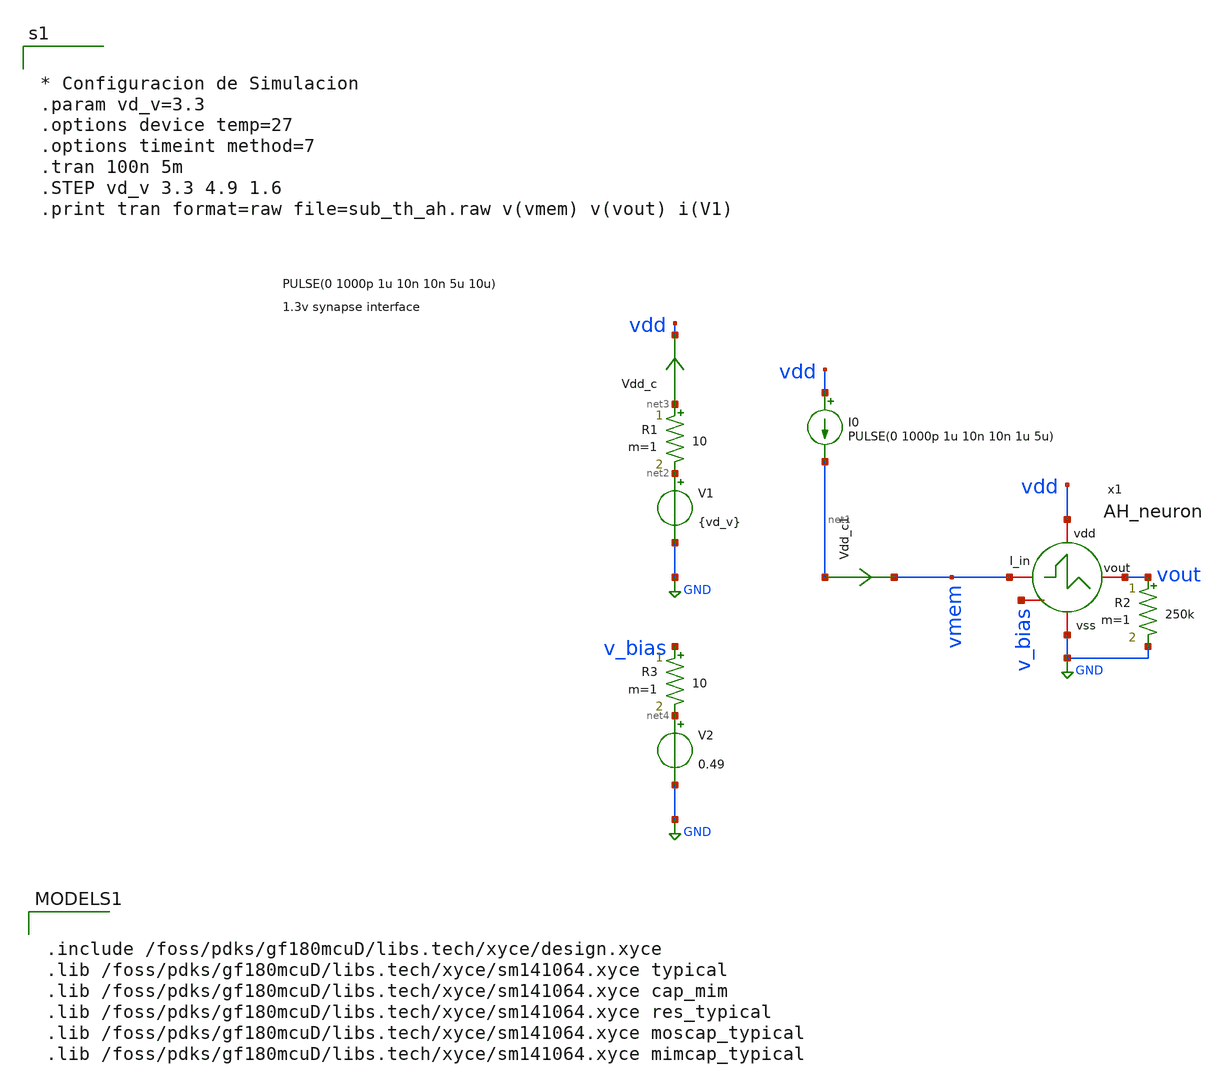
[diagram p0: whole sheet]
** sch_path: designs/libs/tb_core_analogs/tb_AH_neuron/AH_neuron.sch
**.subckt AH_neuron
V1 net2 GND {vd_v}
Vdd_c net3 vdd 0
.save i(vdd_c)
I0 vdd net1 PULSE(0 1000p 1u 10n 10n 1u 5u)
x1 vdd vmem vout GND v_bias AH_neuron
R1 net3 net2 10 m=1
R2 vout GND 250k m=1
Vdd_c1 net1 vmem 0
.save i(vdd_c1)
V2 net4 GND 0.49
R3 v_bias net4 10 m=1
**** begin user architecture code


* Configuracion de Simulacion
.param vd_v=3.3
.options device temp=27
.options timeint method=7
.tran 100n 5m
.STEP vd_v 3.3 4.9 1.6
.print tran format=raw file=sub_th_ah.raw v(vmem) v(vout) i(V1)



.include /foss/pdks/gf180mcuD/libs.tech/xyce/design.xyce
.lib /foss/pdks/gf180mcuD/libs.tech/xyce/sm141064.xyce typical
.lib /foss/pdks/gf180mcuD/libs.tech/xyce/sm141064.xyce cap_mim
.lib /foss/pdks/gf180mcuD/libs.tech/xyce/sm141064.xyce res_typical
.lib /foss/pdks/gf180mcuD/libs.tech/xyce/sm141064.xyce moscap_typical
.lib /foss/pdks/gf180mcuD/libs.tech/xyce/sm141064.xyce mimcap_typical

**** end user architecture code
**.ends
.GLOBAL GND
.end
